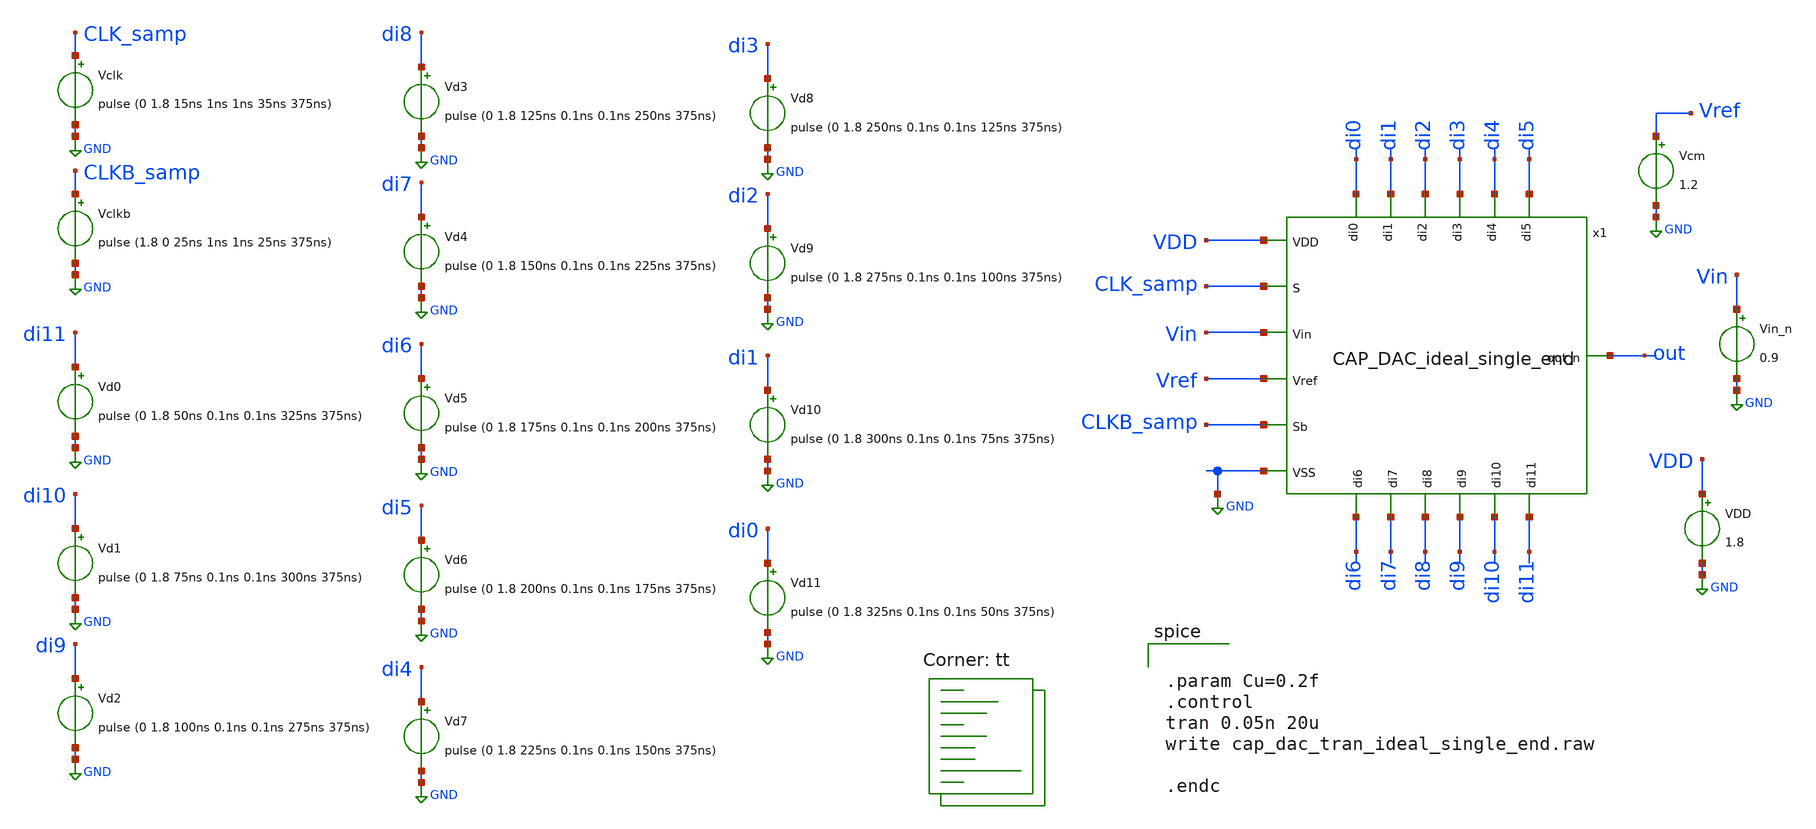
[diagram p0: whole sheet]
** sch_path: CAP_DAC_ideal_single_end_tb.sch
**.subckt CAP_DAC_ideal_single_end_tb
VDD VDD GND 1.8
Vclk CLK_samp GND pulse (0 1.8 15ns 1ns 1ns 35ns 375ns)
Vclkb CLKB_samp GND pulse (1.8 0 25ns 1ns 1ns 25ns 375ns)
Vcm Vref GND 1.2
Vin_n Vin GND 0.9
Vd0 di11 GND pulse (0 1.8 50ns 0.1ns 0.1ns 325ns 375ns)
Vd1 di10 GND pulse (0 1.8 75ns 0.1ns 0.1ns 300ns 375ns)
Vd2 di9 GND pulse (0 1.8 100ns 0.1ns 0.1ns 275ns 375ns)
Vd3 di8 GND pulse (0 1.8 125ns 0.1ns 0.1ns 250ns 375ns)
Vd4 di7 GND pulse (0 1.8 150ns 0.1ns 0.1ns 225ns 375ns)
Vd5 di6 GND pulse (0 1.8 175ns 0.1ns 0.1ns 200ns 375ns)
Vd6 di5 GND pulse (0 1.8 200ns 0.1ns 0.1ns 175ns 375ns)
Vd7 di4 GND pulse (0 1.8 225ns 0.1ns 0.1ns 150ns 375ns)
Vd8 di3 GND pulse (0 1.8 250ns 0.1ns 0.1ns 125ns 375ns)
Vd9 di2 GND pulse (0 1.8 275ns 0.1ns 0.1ns 100ns 375ns)
Vd10 di1 GND pulse (0 1.8 300ns 0.1ns 0.1ns 75ns 375ns)
Vd11 di0 GND pulse (0 1.8 325ns 0.1ns 0.1ns 50ns 375ns)
x1 Vref di0 di1 di2 VDD di3 GND di4 Vin di5 CLK_samp di6 CLKB_samp di7 out di8 di9 di10 di11
+ CAP_DAC_ideal_single_end
**** begin user architecture code
.lib $::SKYWATER_MODELS/sky130.lib.spice tt


.param Cu=0.2f
.control
tran 0.05n 20u
write cap_dac_tran_ideal_single_end.raw

.endc


**** end user architecture code
**.ends
.GLOBAL GND
.end
